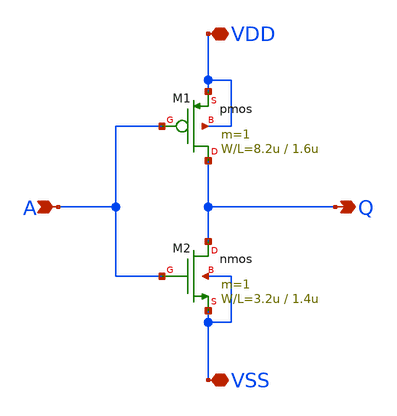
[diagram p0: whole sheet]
** sch_path: member_project/konikoni428/ishi-kai0719.sch
**.subckt ishi-kai0719 A Q VDD VSS
*.ipin A
*.opin Q
*.iopin VDD
*.iopin VSS
M2 Q A VSS VSS nmos L=1.4u W=3.2u m=1
M1 Q A VDD VDD pmos L=1.6u W=8.2u m=1
**.ends
.end
